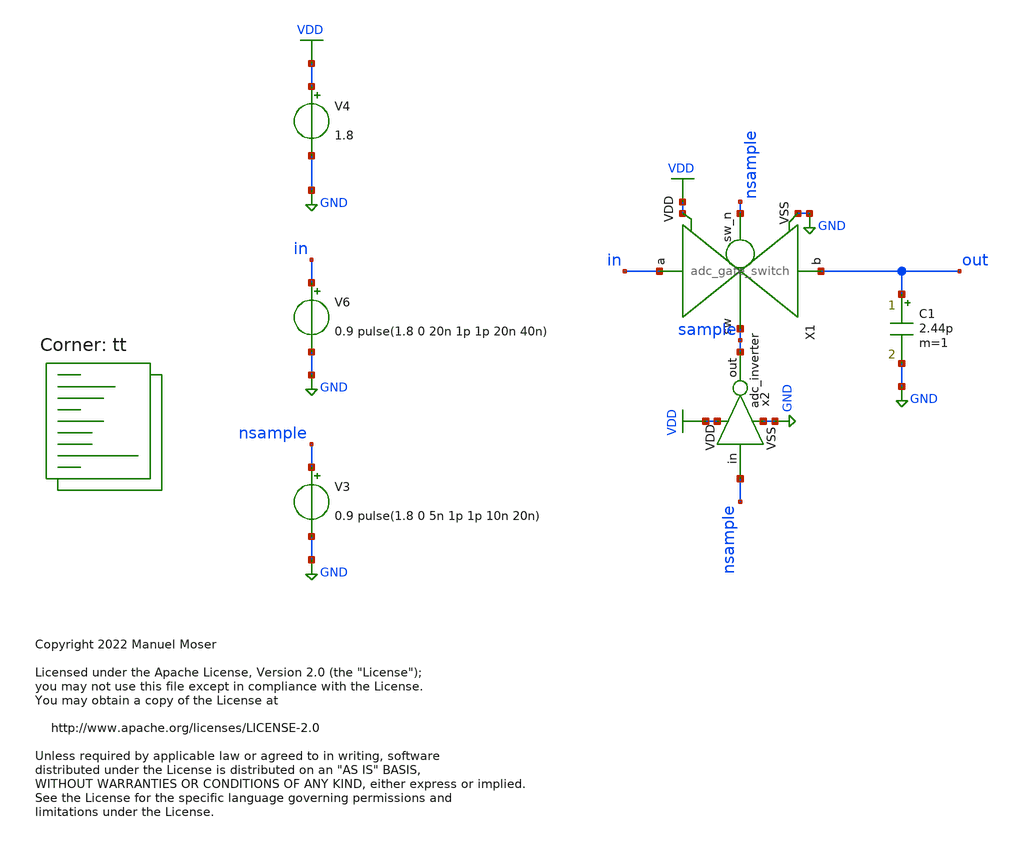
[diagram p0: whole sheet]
** sch_path: xschem/adc_gate_tb_transient.sch
* Copyright 2022 Manuel Moser
* Licensed under the Apache License, Version 2.0 (the "License");
**.subckt adc_gate_tb_transient
X1 nsample in sample out VDD GND adc_gate_switch
V3 nsample GND 0.9 pulse(1.8 0 5n 1p 1p 10n 20n)
V4 VDD GND 1.8
V6 in GND 0.9 pulse(1.8 0 20n 1p 1p 20n 40n)
x2 VDD GND nsample sample adc_inverter
C1 out GND 2.44p m=1
**** begin user architecture code
.lib $::SKYWATER_MODELS/sky130.lib.spice tt


.save all
.temp = 25
*.options method=gear
.OPTIONS savecurrents
.OPTIONS RELTOL=.1 TRTOL=1 ABSTOL=1e-20 CHGTOL=1.0e-20 DEFAD=1.0e-18

.tran 10p 65n

.control
run
plot v(sample) v(in) v(out)
.endc


**** end user architecture code
**.ends
.GLOBAL GND
.GLOBAL VDD
.end
